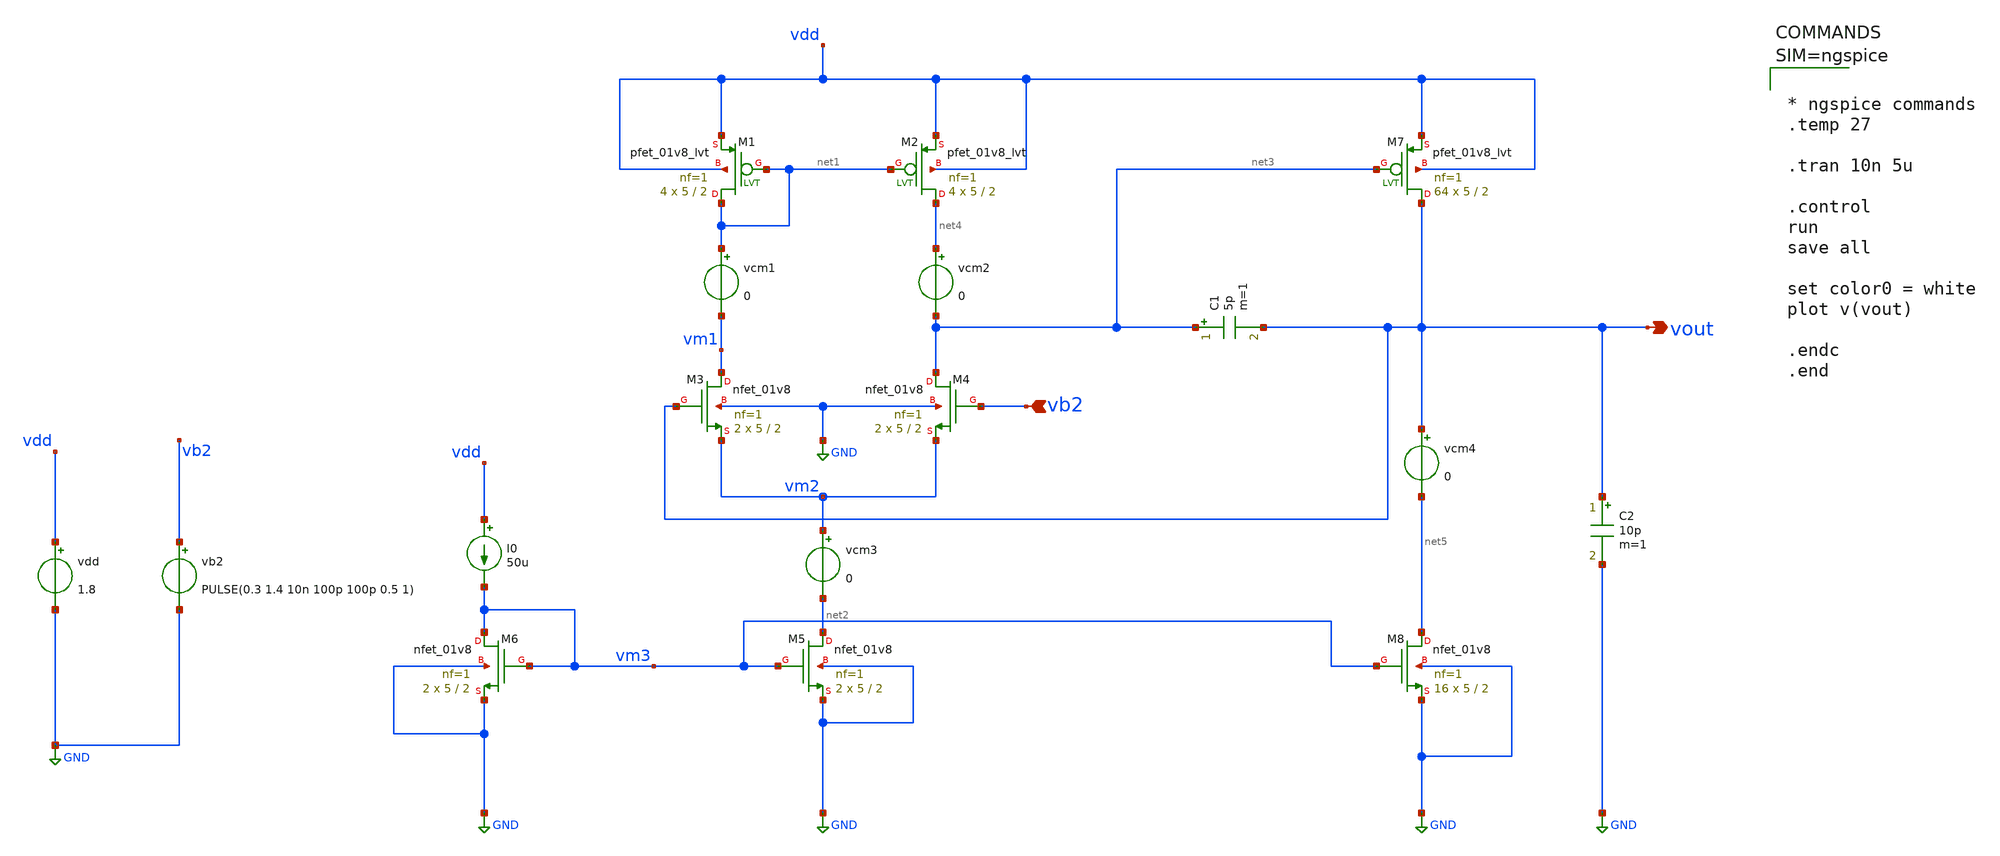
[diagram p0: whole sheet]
** sch_path: testbenches/Two_Stage_Differential_OpAmp_Transient_Analysis.sch
**.subckt Two_Stage_Differential_OpAmp_Transient_Analysis vout vb2
*.opin vout
*.ipin vb2
XM5 net2 vm3 GND GND sky130_fd_pr__nfet_01v8 L=2 W=5 nf=1 ad='int((1 + 1)/2) * 5 / 1 * 0.29' as='int((1 + 2)/2) * 5 / 1 * 0.29'
+ pd='2*int((1 + 1)/2) * (5 / 1 + 0.29)' ps='2*int((1 + 2)/2) * (5 / 1 + 0.29)' nrd='0.29 / 5 ' nrs='0.29 / 5 '
+ sa=0 sb=0 sd=0 mult=2 m=2
I0 vdd vm3 50u
XM2 net4 net1 vdd vdd sky130_fd_pr__pfet_01v8_lvt L=2 W=5 nf=1 ad='int((1 + 1)/2) * 5 / 1 * 0.29' as='int((1 + 2)/2) * 5 / 1 * 0.29'
+ pd='2*int((1 + 1)/2) * (5 / 1 + 0.29)' ps='2*int((1 + 2)/2) * (5 / 1 + 0.29)' nrd='0.29 / 5 ' nrs='0.29 / 5 '
+ sa=0 sb=0 sd=0 mult=4 m=4
XM3 vm1 vout vm2 GND sky130_fd_pr__nfet_01v8 L=2 W=5 nf=1 ad='int((1 + 1)/2) * 5 / 1 * 0.29' as='int((1 + 2)/2) * 5 / 1 * 0.29'
+ pd='2*int((1 + 1)/2) * (5 / 1 + 0.29)' ps='2*int((1 + 2)/2) * (5 / 1 + 0.29)' nrd='0.29 / 5 ' nrs='0.29 / 5 '
+ sa=0 sb=0 sd=0 mult=2 m=2
XM4 net3 vb2 vm2 GND sky130_fd_pr__nfet_01v8 L=2 W=5 nf=1 ad='int((1 + 1)/2) * 5 / 1 * 0.29' as='int((1 + 2)/2) * 5 / 1 * 0.29'
+ pd='2*int((1 + 1)/2) * (5 / 1 + 0.29)' ps='2*int((1 + 2)/2) * (5 / 1 + 0.29)' nrd='0.29 / 5 ' nrs='0.29 / 5 '
+ sa=0 sb=0 sd=0 mult=2 m=2
XM6 vm3 vm3 GND GND sky130_fd_pr__nfet_01v8 L=2 W=5 nf=1 ad='int((1 + 1)/2) * 5 / 1 * 0.29' as='int((1 + 2)/2) * 5 / 1 * 0.29'
+ pd='2*int((1 + 1)/2) * (5 / 1 + 0.29)' ps='2*int((1 + 2)/2) * (5 / 1 + 0.29)' nrd='0.29 / 5 ' nrs='0.29 / 5 '
+ sa=0 sb=0 sd=0 mult=2 m=2
XM1 net1 net1 vdd vdd sky130_fd_pr__pfet_01v8_lvt L=2 W=5 nf=1 ad='int((1 + 1)/2) * 5 / 1 * 0.29' as='int((1 + 2)/2) * 5 / 1 * 0.29'
+ pd='2*int((1 + 1)/2) * (5 / 1 + 0.29)' ps='2*int((1 + 2)/2) * (5 / 1 + 0.29)' nrd='0.29 / 5 ' nrs='0.29 / 5 '
+ sa=0 sb=0 sd=0 mult=4 m=4
vcm3 vm2 net2 0
vcm1 net1 vm1 0
vcm2 net4 net3 0
XM7 vout net3 vdd vdd sky130_fd_pr__pfet_01v8_lvt L=2 W=5 nf=1 ad='int((1 + 1)/2) * 5 / 1 * 0.29' as='int((1 + 2)/2) * 5 / 1 * 0.29'
+ pd='2*int((1 + 1)/2) * (5 / 1 + 0.29)' ps='2*int((1 + 2)/2) * (5 / 1 + 0.29)' nrd='0.29 / 5 ' nrs='0.29 / 5 '
+ sa=0 sb=0 sd=0 mult=64 m=64
XM8 net5 vm3 GND GND sky130_fd_pr__nfet_01v8 L=2 W=5 nf=1 ad='int((1 + 1)/2) * 5 / 1 * 0.29' as='int((1 + 2)/2) * 5 / 1 * 0.29'
+ pd='2*int((1 + 1)/2) * (5 / 1 + 0.29)' ps='2*int((1 + 2)/2) * (5 / 1 + 0.29)' nrd='0.29 / 5 ' nrs='0.29 / 5 '
+ sa=0 sb=0 sd=0 mult=16 m=16
C1 net3 vout 5p m=1
vcm4 vout net5 0
C2 vout GND 10p m=1
vdd vdd GND 1.8
vb2 vb2 GND PULSE(0.3 1.4 10n 100p 100p 0.5 1)
**** begin user architecture code

** opencircuitdesign pdks install
.lib $::SKYWATER_MODELS/sky130.lib.spice tt




* ngspice commands
.temp 27

.tran 10n 5u

.control
run
save all

set color0 = white
plot v(vout)

.endc
.end



**** end user architecture code
**.ends
.GLOBAL GND
.end
